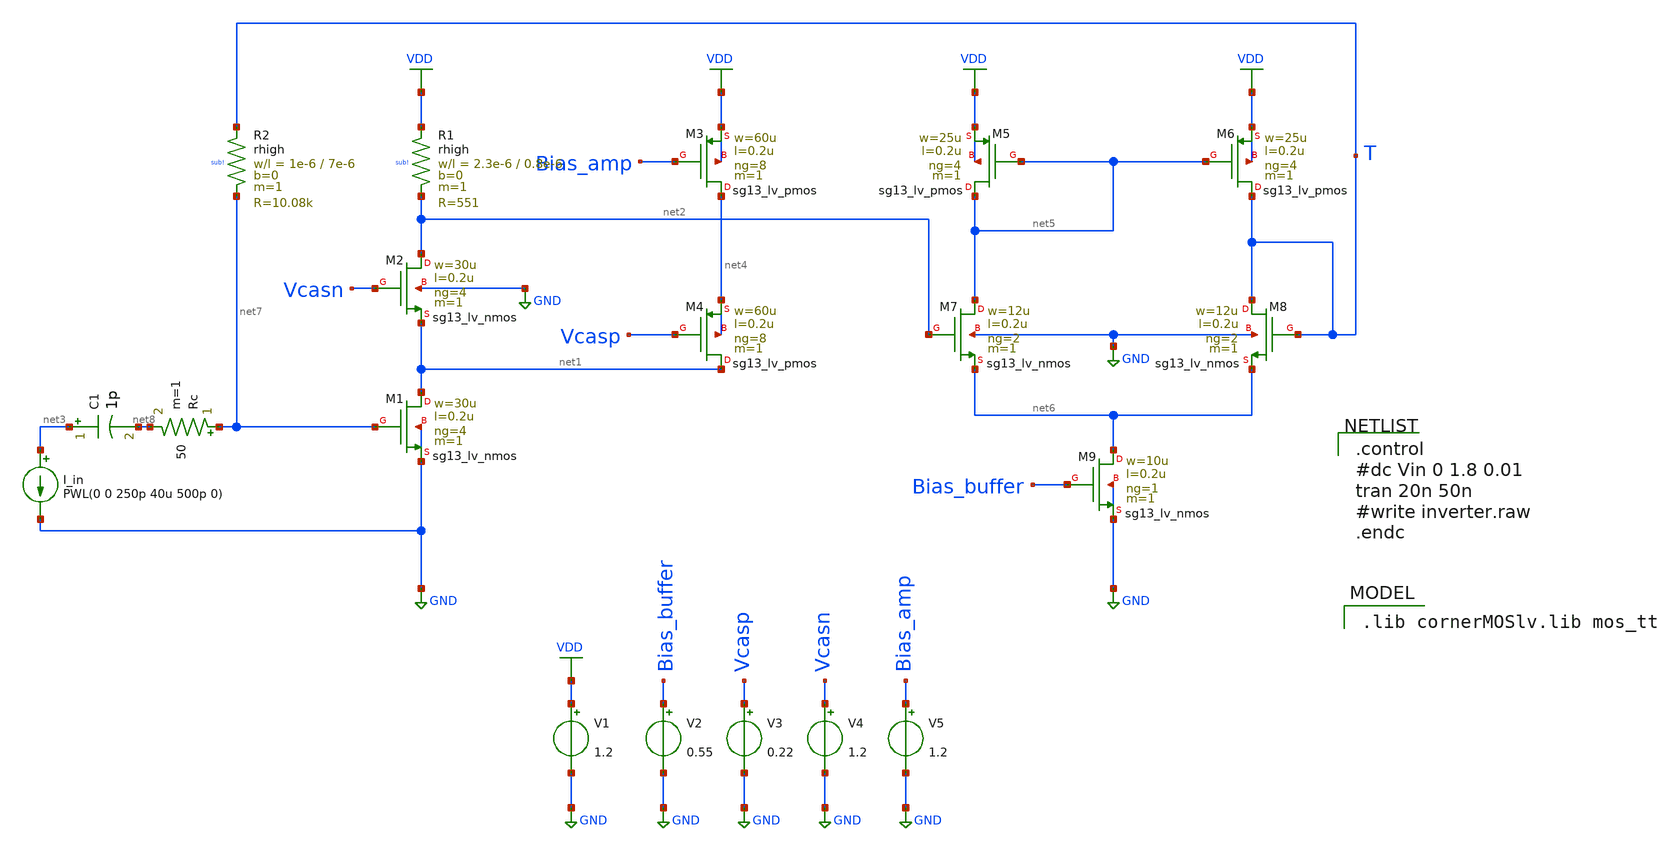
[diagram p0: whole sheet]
** sch_path: FHG_CASCODE_TIA/design_data/xschem/TIA_cascode.sch
**.subckt TIA_cascode
XM1 net1 net7 GND GND sg13_lv_nmos w=30u l=0.2u ng=4 m=1 mm_ok=1
XM2 net2 Vcasn net1 GND sg13_lv_nmos w=30u l=0.2u ng=4 m=1 mm_ok=1
XM3 net4 Bias_amp VDD VDD sg13_lv_pmos w=60u l=0.2u ng=8 m=1 mm_ok=1
XM4 net1 Vcasp net4 net4 sg13_lv_pmos w=60u l=0.2u ng=8 m=1 mm_ok=1
XM5 net5 net5 VDD VDD sg13_lv_pmos w=25u l=0.2u ng=4 m=1 mm_ok=1
XM6 T net5 VDD VDD sg13_lv_pmos w=25u l=0.2u ng=4 m=1 mm_ok=1
XM7 net5 net2 net6 GND sg13_lv_nmos w=12u l=0.2u ng=2 m=1 mm_ok=1
XM8 T T net6 GND sg13_lv_nmos w=12u l=0.2u ng=2 m=1 mm_ok=1
XM9 net6 Bias_buffer GND GND sg13_lv_nmos w=10u l=0.2u ng=1 m=1 mm_ok=1
V1 VDD GND 1.2
I_in net3 GND PWL(0 0 250p 40u 500p 0)
V2 Bias_buffer GND 0.55
V3 Vcasp GND 0.22
V4 Vcasn GND 1.2
V5 Bias_amp GND 1.2
C1 net3 net8 1p m=1
XR2 T net7 sub! rhigh w=1e-6 l=7e-6 m=1 b=0 mm_ok=1
XR1 VDD net2 sub! rhigh w=2.3e-6 l=0.8e-6 m=1 b=0 mm_ok=1
Rc net7 net8 50 m=1
**** begin user architecture code

.control
#dc Vin 0 1.8 0.01
tran 20n 50n
#write inverter.raw
.endc

 .lib cornerMOSlv.lib mos_tt

**** end user architecture code
**.ends
.GLOBAL GND
.GLOBAL VDD
.end
